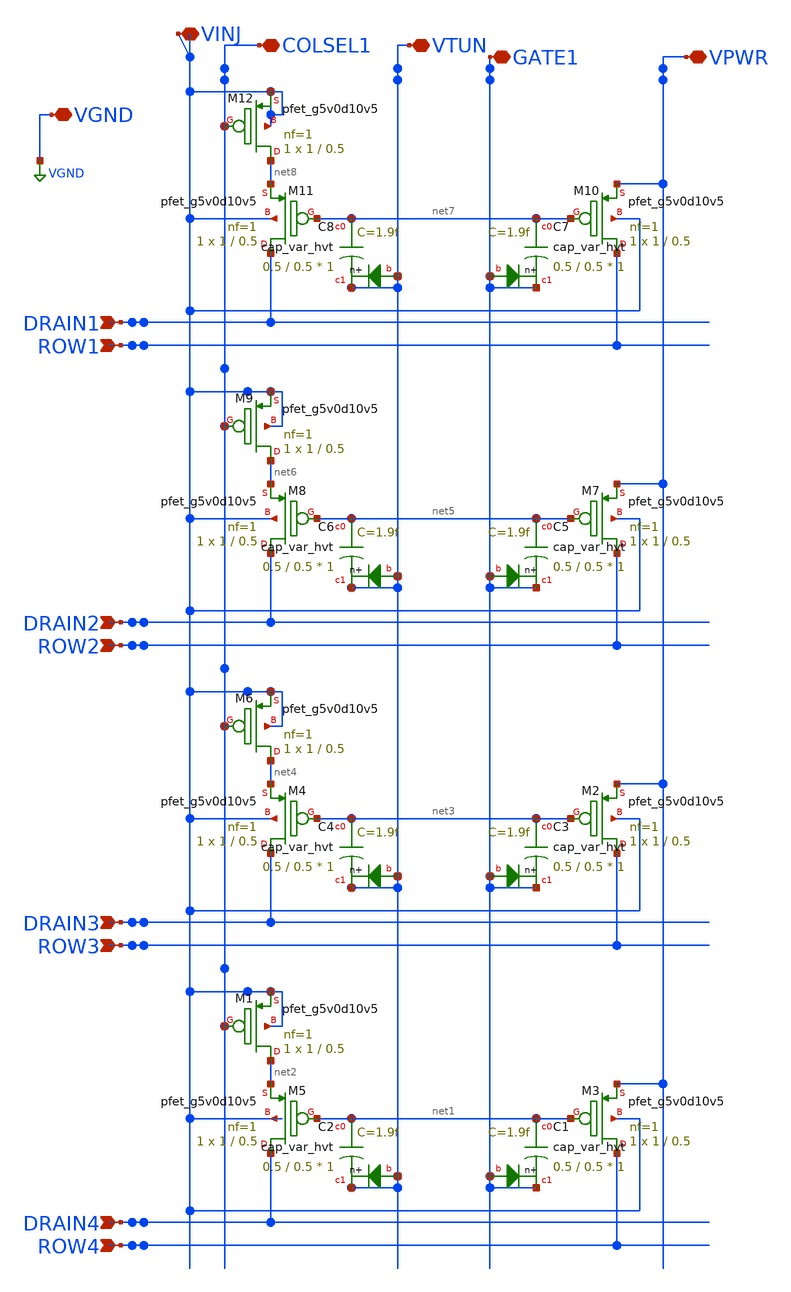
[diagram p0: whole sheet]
** sch_path: libs.ref/sky130_hilas_sc/xschem/sky130_hilas_swc4x1BiasCell.sch
**.subckt sky130_hilas_swc4x1BiasCell DRAIN1 ROW1 DRAIN2 ROW2 DRAIN3 ROW3 DRAIN4 ROW4 VPWR GATE1
*+ VTUN COLSEL1 VINJ VGND
*.ipin DRAIN1
*.ipin ROW1
*.ipin DRAIN2
*.ipin ROW2
*.ipin DRAIN3
*.ipin ROW3
*.ipin DRAIN4
*.ipin ROW4
*.iopin VPWR
*.iopin GATE1
*.iopin VTUN
*.iopin COLSEL1
*.iopin VINJ
*.iopin VGND
XM3 ROW4 net1 VPWR VINJ sky130_fd_pr__pfet_g5v0d10v5 L=0.5 W=1 nf=1 ad='int((nf+1)/2) * W/nf * 0.29'
+ as='int((nf+2)/2) * W/nf * 0.29' pd='2*int((nf+1)/2) * (W/nf + 0.29)' ps='2*int((nf+2)/2) * (W/nf + 0.29)'
+ nrd='0.29 / W' nrs='0.29 / W' sa=0 sb=0 sd=0 mult=1 m=1
XC1 net1 GATE1 GATE1 sky130_fd_pr__cap_var_hvt W=0.5 L=0.5 VM=1 m=1
XM5 DRAIN4 net1 net2 VINJ sky130_fd_pr__pfet_g5v0d10v5 L=0.5 W=1 nf=1 ad='int((nf+1)/2) * W/nf * 0.29'
+ as='int((nf+2)/2) * W/nf * 0.29' pd='2*int((nf+1)/2) * (W/nf + 0.29)' ps='2*int((nf+2)/2) * (W/nf + 0.29)'
+ nrd='0.29 / W' nrs='0.29 / W' sa=0 sb=0 sd=0 mult=1 m=1
XC2 net1 VTUN VTUN sky130_fd_pr__cap_var_hvt W=0.5 L=0.5 VM=1 m=1
XM1 net2 COLSEL1 VINJ VINJ sky130_fd_pr__pfet_g5v0d10v5 L=0.5 W=1 nf=1 ad='int((nf+1)/2) * W/nf * 0.29'
+ as='int((nf+2)/2) * W/nf * 0.29' pd='2*int((nf+1)/2) * (W/nf + 0.29)' ps='2*int((nf+2)/2) * (W/nf + 0.29)'
+ nrd='0.29 / W' nrs='0.29 / W' sa=0 sb=0 sd=0 mult=1 m=1
XM2 ROW3 net3 VPWR VINJ sky130_fd_pr__pfet_g5v0d10v5 L=0.5 W=1 nf=1 ad='int((nf+1)/2) * W/nf * 0.29'
+ as='int((nf+2)/2) * W/nf * 0.29' pd='2*int((nf+1)/2) * (W/nf + 0.29)' ps='2*int((nf+2)/2) * (W/nf + 0.29)'
+ nrd='0.29 / W' nrs='0.29 / W' sa=0 sb=0 sd=0 mult=1 m=1
XC3 net3 GATE1 GATE1 sky130_fd_pr__cap_var_hvt W=0.5 L=0.5 VM=1 m=1
XM4 DRAIN3 net3 net4 VINJ sky130_fd_pr__pfet_g5v0d10v5 L=0.5 W=1 nf=1 ad='int((nf+1)/2) * W/nf * 0.29'
+ as='int((nf+2)/2) * W/nf * 0.29' pd='2*int((nf+1)/2) * (W/nf + 0.29)' ps='2*int((nf+2)/2) * (W/nf + 0.29)'
+ nrd='0.29 / W' nrs='0.29 / W' sa=0 sb=0 sd=0 mult=1 m=1
XC4 net3 VTUN VTUN sky130_fd_pr__cap_var_hvt W=0.5 L=0.5 VM=1 m=1
XM6 net4 COLSEL1 VINJ VINJ sky130_fd_pr__pfet_g5v0d10v5 L=0.5 W=1 nf=1 ad='int((nf+1)/2) * W/nf * 0.29'
+ as='int((nf+2)/2) * W/nf * 0.29' pd='2*int((nf+1)/2) * (W/nf + 0.29)' ps='2*int((nf+2)/2) * (W/nf + 0.29)'
+ nrd='0.29 / W' nrs='0.29 / W' sa=0 sb=0 sd=0 mult=1 m=1
XM7 ROW2 net5 VPWR VINJ sky130_fd_pr__pfet_g5v0d10v5 L=0.5 W=1 nf=1 ad='int((nf+1)/2) * W/nf * 0.29'
+ as='int((nf+2)/2) * W/nf * 0.29' pd='2*int((nf+1)/2) * (W/nf + 0.29)' ps='2*int((nf+2)/2) * (W/nf + 0.29)'
+ nrd='0.29 / W' nrs='0.29 / W' sa=0 sb=0 sd=0 mult=1 m=1
XC5 net5 GATE1 GATE1 sky130_fd_pr__cap_var_hvt W=0.5 L=0.5 VM=1 m=1
XM8 DRAIN2 net5 net6 VINJ sky130_fd_pr__pfet_g5v0d10v5 L=0.5 W=1 nf=1 ad='int((nf+1)/2) * W/nf * 0.29'
+ as='int((nf+2)/2) * W/nf * 0.29' pd='2*int((nf+1)/2) * (W/nf + 0.29)' ps='2*int((nf+2)/2) * (W/nf + 0.29)'
+ nrd='0.29 / W' nrs='0.29 / W' sa=0 sb=0 sd=0 mult=1 m=1
XC6 net5 VTUN VTUN sky130_fd_pr__cap_var_hvt W=0.5 L=0.5 VM=1 m=1
XM9 net6 COLSEL1 VINJ VINJ sky130_fd_pr__pfet_g5v0d10v5 L=0.5 W=1 nf=1 ad='int((nf+1)/2) * W/nf * 0.29'
+ as='int((nf+2)/2) * W/nf * 0.29' pd='2*int((nf+1)/2) * (W/nf + 0.29)' ps='2*int((nf+2)/2) * (W/nf + 0.29)'
+ nrd='0.29 / W' nrs='0.29 / W' sa=0 sb=0 sd=0 mult=1 m=1
XM10 ROW1 net7 VPWR VINJ sky130_fd_pr__pfet_g5v0d10v5 L=0.5 W=1 nf=1 ad='int((nf+1)/2) * W/nf * 0.29'
+ as='int((nf+2)/2) * W/nf * 0.29' pd='2*int((nf+1)/2) * (W/nf + 0.29)' ps='2*int((nf+2)/2) * (W/nf + 0.29)'
+ nrd='0.29 / W' nrs='0.29 / W' sa=0 sb=0 sd=0 mult=1 m=1
XC7 net7 GATE1 GATE1 sky130_fd_pr__cap_var_hvt W=0.5 L=0.5 VM=1 m=1
XM11 DRAIN1 net7 net8 VINJ sky130_fd_pr__pfet_g5v0d10v5 L=0.5 W=1 nf=1 ad='int((nf+1)/2) * W/nf * 0.29'
+ as='int((nf+2)/2) * W/nf * 0.29' pd='2*int((nf+1)/2) * (W/nf + 0.29)' ps='2*int((nf+2)/2) * (W/nf + 0.29)'
+ nrd='0.29 / W' nrs='0.29 / W' sa=0 sb=0 sd=0 mult=1 m=1
XC8 net7 VTUN VTUN sky130_fd_pr__cap_var_hvt W=0.5 L=0.5 VM=1 m=1
XM12 net8 COLSEL1 VINJ VINJ sky130_fd_pr__pfet_g5v0d10v5 L=0.5 W=1 nf=1 ad='int((nf+1)/2) * W/nf * 0.29'
+ as='int((nf+2)/2) * W/nf * 0.29' pd='2*int((nf+1)/2) * (W/nf + 0.29)' ps='2*int((nf+2)/2) * (W/nf + 0.29)'
+ nrd='0.29 / W' nrs='0.29 / W' sa=0 sb=0 sd=0 mult=1 m=1
**.ends
.GLOBAL VGND
.end
